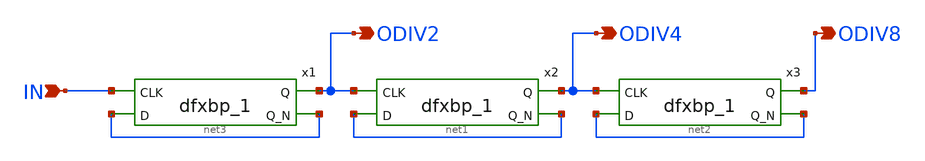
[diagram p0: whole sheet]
** sch_path: xschem/freq_divider.sch
**.subckt freq_divider IN ODIV2 ODIV4 ODIV8
*.ipin IN
*.opin ODIV2
*.opin ODIV4
*.opin ODIV8
x1 IN net3 VGND VNB VPB VPWR ODIV2 net3 sky130_fd_sc_hd__dfxbp_1
x2 ODIV2 net1 VGND VNB VPB VPWR ODIV4 net1 sky130_fd_sc_hd__dfxbp_1
x3 ODIV4 net2 VGND VNB VPB VPWR ODIV8 net2 sky130_fd_sc_hd__dfxbp_1
**.ends
.end
